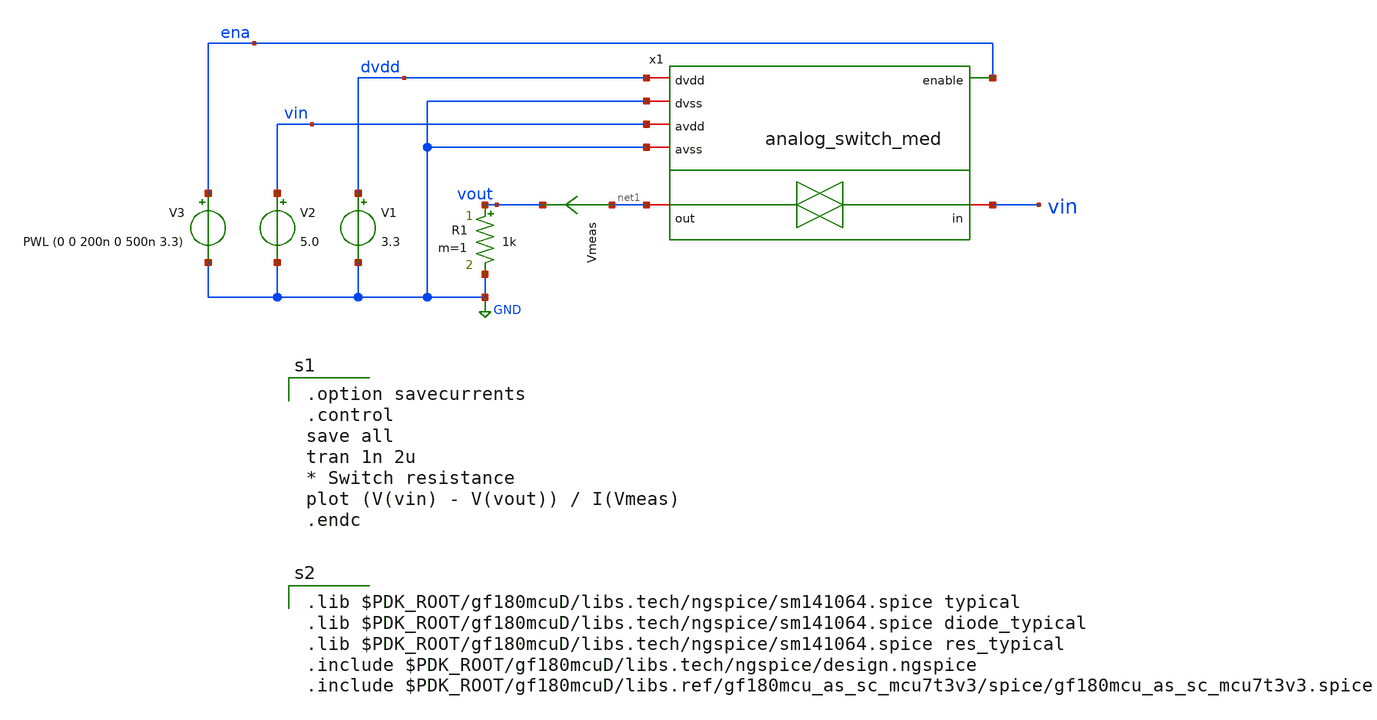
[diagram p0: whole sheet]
** sch_path: xschem/analog_switch_med_tb.sch
**.subckt analog_switch_med_tb
Vmeas net1 vout 0
.save i(vmeas)
R1 vout GND 1k m=1
V1 dvdd GND 3.3
V2 vin GND 5.0
V3 ena GND PWL (0 0 200n 0 500n 3.3)
x1 dvdd GND vin vin GND ena net1 analog_switch_med
**** begin user architecture code

.option savecurrents
.control
save all
tran 1n 2u
* Switch resistance
plot (V(vin) - V(vout)) / I(Vmeas)
.endc


.lib $PDK_ROOT/gf180mcuD/libs.tech/ngspice/sm141064.spice typical
.lib $PDK_ROOT/gf180mcuD/libs.tech/ngspice/sm141064.spice diode_typical
.lib $PDK_ROOT/gf180mcuD/libs.tech/ngspice/sm141064.spice res_typical
.include $PDK_ROOT/gf180mcuD/libs.tech/ngspice/design.ngspice
.include $PDK_ROOT/gf180mcuD/libs.ref/gf180mcu_as_sc_mcu7t3v3/spice/gf180mcu_as_sc_mcu7t3v3.spice

**** end user architecture code
**.ends
.GLOBAL GND
.end
